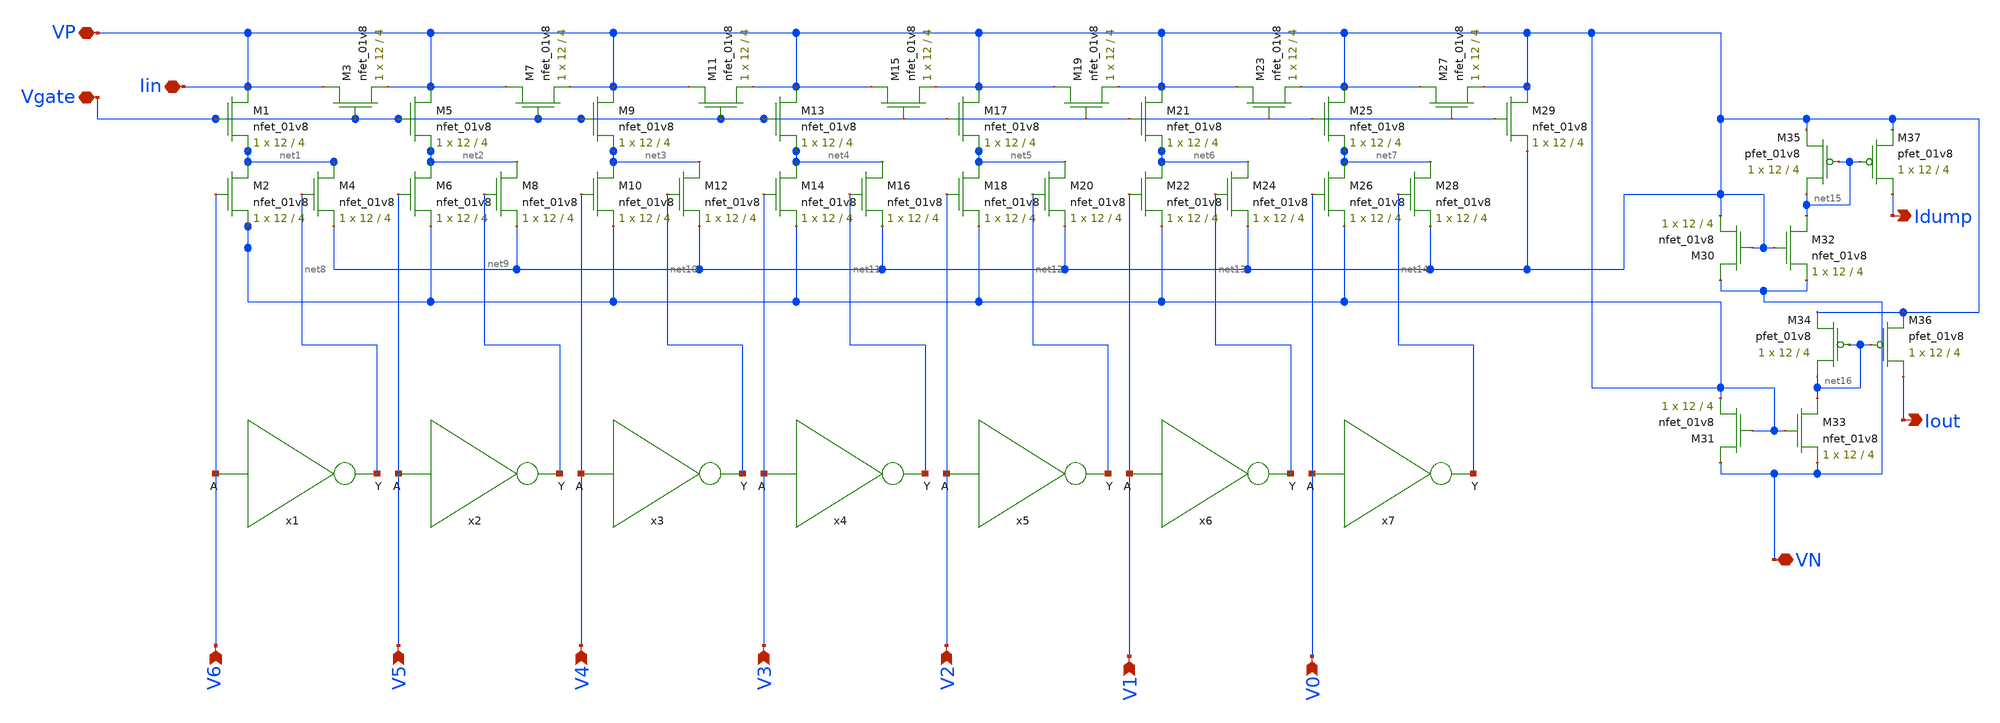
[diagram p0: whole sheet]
** sch_path: xschem/ladder_andrew.sch
**.subckt ladder_andrew V6 V5 V4 V3 V2 V1 V0 VP Iin Iout Idump VN Vgate
*.ipin V6
*.ipin V5
*.ipin V4
*.ipin V3
*.ipin V2
*.ipin V1
*.ipin V0
*.iopin VP
*.iopin Iin
*.opin Iout
*.opin Idump
*.iopin VN
*.iopin Vgate
XM1 VP Vgate net1 GND sky130_fd_pr__nfet_01v8 L=4 W=12 nf=1 ad='int((nf+1)/2) * W/nf * 0.29' as='int((nf+2)/2) * W/nf * 0.29'
+ pd='2*int((nf+1)/2) * (W/nf + 0.29)' ps='2*int((nf+2)/2) * (W/nf + 0.29)' nrd='0.29 / W' nrs='0.29 / W'
+ sa=0 sb=0 sd=0 mult=1 m=1
XM3 VP Vgate VP GND sky130_fd_pr__nfet_01v8 L=4 W=12 nf=1 ad='int((nf+1)/2) * W/nf * 0.29' as='int((nf+2)/2) * W/nf * 0.29'
+ pd='2*int((nf+1)/2) * (W/nf + 0.29)' ps='2*int((nf+2)/2) * (W/nf + 0.29)' nrd='0.29 / W' nrs='0.29 / W'
+ sa=0 sb=0 sd=0 mult=1 m=1
XM5 VP Vgate net2 GND sky130_fd_pr__nfet_01v8 L=4 W=12 nf=1 ad='int((nf+1)/2) * W/nf * 0.29' as='int((nf+2)/2) * W/nf * 0.29'
+ pd='2*int((nf+1)/2) * (W/nf + 0.29)' ps='2*int((nf+2)/2) * (W/nf + 0.29)' nrd='0.29 / W' nrs='0.29 / W'
+ sa=0 sb=0 sd=0 mult=1 m=1
XM7 VP Vgate VP GND sky130_fd_pr__nfet_01v8 L=4 W=12 nf=1 ad='int((nf+1)/2) * W/nf * 0.29' as='int((nf+2)/2) * W/nf * 0.29'
+ pd='2*int((nf+1)/2) * (W/nf + 0.29)' ps='2*int((nf+2)/2) * (W/nf + 0.29)' nrd='0.29 / W' nrs='0.29 / W'
+ sa=0 sb=0 sd=0 mult=1 m=1
XM6 net2 V5 VP GND sky130_fd_pr__nfet_01v8 L=4 W=12 nf=1 ad='int((nf+1)/2) * W/nf * 0.29' as='int((nf+2)/2) * W/nf * 0.29'
+ pd='2*int((nf+1)/2) * (W/nf + 0.29)' ps='2*int((nf+2)/2) * (W/nf + 0.29)' nrd='0.29 / W' nrs='0.29 / W'
+ sa=0 sb=0 sd=0 mult=1 m=1
XM8 net2 net9 VP GND sky130_fd_pr__nfet_01v8 L=4 W=12 nf=1 ad='int((nf+1)/2) * W/nf * 0.29' as='int((nf+2)/2) * W/nf * 0.29'
+ pd='2*int((nf+1)/2) * (W/nf + 0.29)' ps='2*int((nf+2)/2) * (W/nf + 0.29)' nrd='0.29 / W' nrs='0.29 / W'
+ sa=0 sb=0 sd=0 mult=1 m=1
XM2 net1 V6 VP GND sky130_fd_pr__nfet_01v8 L=4 W=12 nf=1 ad='int((nf+1)/2) * W/nf * 0.29' as='int((nf+2)/2) * W/nf * 0.29'
+ pd='2*int((nf+1)/2) * (W/nf + 0.29)' ps='2*int((nf+2)/2) * (W/nf + 0.29)' nrd='0.29 / W' nrs='0.29 / W'
+ sa=0 sb=0 sd=0 mult=1 m=1
XM4 net1 net8 VP GND sky130_fd_pr__nfet_01v8 L=4 W=12 nf=1 ad='int((nf+1)/2) * W/nf * 0.29' as='int((nf+2)/2) * W/nf * 0.29'
+ pd='2*int((nf+1)/2) * (W/nf + 0.29)' ps='2*int((nf+2)/2) * (W/nf + 0.29)' nrd='0.29 / W' nrs='0.29 / W'
+ sa=0 sb=0 sd=0 mult=1 m=1
XM9 VP Vgate net3 GND sky130_fd_pr__nfet_01v8 L=4 W=12 nf=1 ad='int((nf+1)/2) * W/nf * 0.29' as='int((nf+2)/2) * W/nf * 0.29'
+ pd='2*int((nf+1)/2) * (W/nf + 0.29)' ps='2*int((nf+2)/2) * (W/nf + 0.29)' nrd='0.29 / W' nrs='0.29 / W'
+ sa=0 sb=0 sd=0 mult=1 m=1
XM11 VP Vgate VP GND sky130_fd_pr__nfet_01v8 L=4 W=12 nf=1 ad='int((nf+1)/2) * W/nf * 0.29' as='int((nf+2)/2) * W/nf * 0.29'
+ pd='2*int((nf+1)/2) * (W/nf + 0.29)' ps='2*int((nf+2)/2) * (W/nf + 0.29)' nrd='0.29 / W' nrs='0.29 / W'
+ sa=0 sb=0 sd=0 mult=1 m=1
XM10 net3 V4 VP GND sky130_fd_pr__nfet_01v8 L=4 W=12 nf=1 ad='int((nf+1)/2) * W/nf * 0.29' as='int((nf+2)/2) * W/nf * 0.29'
+ pd='2*int((nf+1)/2) * (W/nf + 0.29)' ps='2*int((nf+2)/2) * (W/nf + 0.29)' nrd='0.29 / W' nrs='0.29 / W'
+ sa=0 sb=0 sd=0 mult=1 m=1
XM12 net3 net10 VP GND sky130_fd_pr__nfet_01v8 L=4 W=12 nf=1 ad='int((nf+1)/2) * W/nf * 0.29' as='int((nf+2)/2) * W/nf * 0.29'
+ pd='2*int((nf+1)/2) * (W/nf + 0.29)' ps='2*int((nf+2)/2) * (W/nf + 0.29)' nrd='0.29 / W' nrs='0.29 / W'
+ sa=0 sb=0 sd=0 mult=1 m=1
XM13 VP Vgate net4 GND sky130_fd_pr__nfet_01v8 L=4 W=12 nf=1 ad='int((nf+1)/2) * W/nf * 0.29' as='int((nf+2)/2) * W/nf * 0.29'
+ pd='2*int((nf+1)/2) * (W/nf + 0.29)' ps='2*int((nf+2)/2) * (W/nf + 0.29)' nrd='0.29 / W' nrs='0.29 / W'
+ sa=0 sb=0 sd=0 mult=1 m=1
XM15 VP Vgate VP GND sky130_fd_pr__nfet_01v8 L=4 W=12 nf=1 ad='int((nf+1)/2) * W/nf * 0.29' as='int((nf+2)/2) * W/nf * 0.29'
+ pd='2*int((nf+1)/2) * (W/nf + 0.29)' ps='2*int((nf+2)/2) * (W/nf + 0.29)' nrd='0.29 / W' nrs='0.29 / W'
+ sa=0 sb=0 sd=0 mult=1 m=1
XM14 net4 V3 VP GND sky130_fd_pr__nfet_01v8 L=4 W=12 nf=1 ad='int((nf+1)/2) * W/nf * 0.29' as='int((nf+2)/2) * W/nf * 0.29'
+ pd='2*int((nf+1)/2) * (W/nf + 0.29)' ps='2*int((nf+2)/2) * (W/nf + 0.29)' nrd='0.29 / W' nrs='0.29 / W'
+ sa=0 sb=0 sd=0 mult=1 m=1
XM16 net4 net11 VP GND sky130_fd_pr__nfet_01v8 L=4 W=12 nf=1 ad='int((nf+1)/2) * W/nf * 0.29' as='int((nf+2)/2) * W/nf * 0.29'
+ pd='2*int((nf+1)/2) * (W/nf + 0.29)' ps='2*int((nf+2)/2) * (W/nf + 0.29)' nrd='0.29 / W' nrs='0.29 / W'
+ sa=0 sb=0 sd=0 mult=1 m=1
XM17 VP Vgate net5 GND sky130_fd_pr__nfet_01v8 L=4 W=12 nf=1 ad='int((nf+1)/2) * W/nf * 0.29' as='int((nf+2)/2) * W/nf * 0.29'
+ pd='2*int((nf+1)/2) * (W/nf + 0.29)' ps='2*int((nf+2)/2) * (W/nf + 0.29)' nrd='0.29 / W' nrs='0.29 / W'
+ sa=0 sb=0 sd=0 mult=1 m=1
XM19 VP Vgate VP GND sky130_fd_pr__nfet_01v8 L=4 W=12 nf=1 ad='int((nf+1)/2) * W/nf * 0.29' as='int((nf+2)/2) * W/nf * 0.29'
+ pd='2*int((nf+1)/2) * (W/nf + 0.29)' ps='2*int((nf+2)/2) * (W/nf + 0.29)' nrd='0.29 / W' nrs='0.29 / W'
+ sa=0 sb=0 sd=0 mult=1 m=1
XM18 net5 V2 VP GND sky130_fd_pr__nfet_01v8 L=4 W=12 nf=1 ad='int((nf+1)/2) * W/nf * 0.29' as='int((nf+2)/2) * W/nf * 0.29'
+ pd='2*int((nf+1)/2) * (W/nf + 0.29)' ps='2*int((nf+2)/2) * (W/nf + 0.29)' nrd='0.29 / W' nrs='0.29 / W'
+ sa=0 sb=0 sd=0 mult=1 m=1
XM20 net5 net12 VP GND sky130_fd_pr__nfet_01v8 L=4 W=12 nf=1 ad='int((nf+1)/2) * W/nf * 0.29' as='int((nf+2)/2) * W/nf * 0.29'
+ pd='2*int((nf+1)/2) * (W/nf + 0.29)' ps='2*int((nf+2)/2) * (W/nf + 0.29)' nrd='0.29 / W' nrs='0.29 / W'
+ sa=0 sb=0 sd=0 mult=1 m=1
XM21 VP Vgate net6 GND sky130_fd_pr__nfet_01v8 L=4 W=12 nf=1 ad='int((nf+1)/2) * W/nf * 0.29' as='int((nf+2)/2) * W/nf * 0.29'
+ pd='2*int((nf+1)/2) * (W/nf + 0.29)' ps='2*int((nf+2)/2) * (W/nf + 0.29)' nrd='0.29 / W' nrs='0.29 / W'
+ sa=0 sb=0 sd=0 mult=1 m=1
XM23 VP Vgate VP GND sky130_fd_pr__nfet_01v8 L=4 W=12 nf=1 ad='int((nf+1)/2) * W/nf * 0.29' as='int((nf+2)/2) * W/nf * 0.29'
+ pd='2*int((nf+1)/2) * (W/nf + 0.29)' ps='2*int((nf+2)/2) * (W/nf + 0.29)' nrd='0.29 / W' nrs='0.29 / W'
+ sa=0 sb=0 sd=0 mult=1 m=1
XM22 net6 V1 VP GND sky130_fd_pr__nfet_01v8 L=4 W=12 nf=1 ad='int((nf+1)/2) * W/nf * 0.29' as='int((nf+2)/2) * W/nf * 0.29'
+ pd='2*int((nf+1)/2) * (W/nf + 0.29)' ps='2*int((nf+2)/2) * (W/nf + 0.29)' nrd='0.29 / W' nrs='0.29 / W'
+ sa=0 sb=0 sd=0 mult=1 m=1
XM24 net6 net13 VP GND sky130_fd_pr__nfet_01v8 L=4 W=12 nf=1 ad='int((nf+1)/2) * W/nf * 0.29' as='int((nf+2)/2) * W/nf * 0.29'
+ pd='2*int((nf+1)/2) * (W/nf + 0.29)' ps='2*int((nf+2)/2) * (W/nf + 0.29)' nrd='0.29 / W' nrs='0.29 / W'
+ sa=0 sb=0 sd=0 mult=1 m=1
XM25 VP Vgate net7 GND sky130_fd_pr__nfet_01v8 L=4 W=12 nf=1 ad='int((nf+1)/2) * W/nf * 0.29' as='int((nf+2)/2) * W/nf * 0.29'
+ pd='2*int((nf+1)/2) * (W/nf + 0.29)' ps='2*int((nf+2)/2) * (W/nf + 0.29)' nrd='0.29 / W' nrs='0.29 / W'
+ sa=0 sb=0 sd=0 mult=1 m=1
XM27 VP Vgate VP GND sky130_fd_pr__nfet_01v8 L=4 W=12 nf=1 ad='int((nf+1)/2) * W/nf * 0.29' as='int((nf+2)/2) * W/nf * 0.29'
+ pd='2*int((nf+1)/2) * (W/nf + 0.29)' ps='2*int((nf+2)/2) * (W/nf + 0.29)' nrd='0.29 / W' nrs='0.29 / W'
+ sa=0 sb=0 sd=0 mult=1 m=1
XM26 net7 V0 VP GND sky130_fd_pr__nfet_01v8 L=4 W=12 nf=1 ad='int((nf+1)/2) * W/nf * 0.29' as='int((nf+2)/2) * W/nf * 0.29'
+ pd='2*int((nf+1)/2) * (W/nf + 0.29)' ps='2*int((nf+2)/2) * (W/nf + 0.29)' nrd='0.29 / W' nrs='0.29 / W'
+ sa=0 sb=0 sd=0 mult=1 m=1
XM28 net7 net14 VP GND sky130_fd_pr__nfet_01v8 L=4 W=12 nf=1 ad='int((nf+1)/2) * W/nf * 0.29' as='int((nf+2)/2) * W/nf * 0.29'
+ pd='2*int((nf+1)/2) * (W/nf + 0.29)' ps='2*int((nf+2)/2) * (W/nf + 0.29)' nrd='0.29 / W' nrs='0.29 / W'
+ sa=0 sb=0 sd=0 mult=1 m=1
XM29 VP Vgate VP GND sky130_fd_pr__nfet_01v8 L=4 W=12 nf=1 ad='int((nf+1)/2) * W/nf * 0.29' as='int((nf+2)/2) * W/nf * 0.29'
+ pd='2*int((nf+1)/2) * (W/nf + 0.29)' ps='2*int((nf+2)/2) * (W/nf + 0.29)' nrd='0.29 / W' nrs='0.29 / W'
+ sa=0 sb=0 sd=0 mult=1 m=1
x1 net8 V6 inverter
x2 net9 V5 inverter
x3 net10 V4 inverter
x4 net11 V3 inverter
x5 net12 V2 inverter
x6 net13 V1 inverter
x7 net14 V0 inverter
XM30 VN VP VP GND sky130_fd_pr__nfet_01v8 L=4 W=12 nf=1 ad='int((nf+1)/2) * W/nf * 0.29' as='int((nf+2)/2) * W/nf * 0.29'
+ pd='2*int((nf+1)/2) * (W/nf + 0.29)' ps='2*int((nf+2)/2) * (W/nf + 0.29)' nrd='0.29 / W' nrs='0.29 / W'
+ sa=0 sb=0 sd=0 mult=1 m=1
XM31 VN VP VP GND sky130_fd_pr__nfet_01v8 L=4 W=12 nf=1 ad='int((nf+1)/2) * W/nf * 0.29' as='int((nf+2)/2) * W/nf * 0.29'
+ pd='2*int((nf+1)/2) * (W/nf + 0.29)' ps='2*int((nf+2)/2) * (W/nf + 0.29)' nrd='0.29 / W' nrs='0.29 / W'
+ sa=0 sb=0 sd=0 mult=1 m=1
XM32 net15 VP VN GND sky130_fd_pr__nfet_01v8 L=4 W=12 nf=1 ad='int((nf+1)/2) * W/nf * 0.29' as='int((nf+2)/2) * W/nf * 0.29'
+ pd='2*int((nf+1)/2) * (W/nf + 0.29)' ps='2*int((nf+2)/2) * (W/nf + 0.29)' nrd='0.29 / W' nrs='0.29 / W'
+ sa=0 sb=0 sd=0 mult=1 m=1
XM33 net16 VP VN GND sky130_fd_pr__nfet_01v8 L=4 W=12 nf=1 ad='int((nf+1)/2) * W/nf * 0.29' as='int((nf+2)/2) * W/nf * 0.29'
+ pd='2*int((nf+1)/2) * (W/nf + 0.29)' ps='2*int((nf+2)/2) * (W/nf + 0.29)' nrd='0.29 / W' nrs='0.29 / W'
+ sa=0 sb=0 sd=0 mult=1 m=1
XM35 net15 net15 VP VDD sky130_fd_pr__pfet_01v8 L=4 W=12 nf=1 ad='int((nf+1)/2) * W/nf * 0.29' as='int((nf+2)/2) * W/nf * 0.29'
+ pd='2*int((nf+1)/2) * (W/nf + 0.29)' ps='2*int((nf+2)/2) * (W/nf + 0.29)' nrd='0.29 / W' nrs='0.29 / W'
+ sa=0 sb=0 sd=0 mult=1 m=1
XM37 Idump net15 VP VDD sky130_fd_pr__pfet_01v8 L=4 W=12 nf=1 ad='int((nf+1)/2) * W/nf * 0.29' as='int((nf+2)/2) * W/nf * 0.29'
+ pd='2*int((nf+1)/2) * (W/nf + 0.29)' ps='2*int((nf+2)/2) * (W/nf + 0.29)' nrd='0.29 / W' nrs='0.29 / W'
+ sa=0 sb=0 sd=0 mult=1 m=1
XM34 net16 net16 VP VDD sky130_fd_pr__pfet_01v8 L=4 W=12 nf=1 ad='int((nf+1)/2) * W/nf * 0.29' as='int((nf+2)/2) * W/nf * 0.29'
+ pd='2*int((nf+1)/2) * (W/nf + 0.29)' ps='2*int((nf+2)/2) * (W/nf + 0.29)' nrd='0.29 / W' nrs='0.29 / W'
+ sa=0 sb=0 sd=0 mult=1 m=1
XM36 Iout net16 VP VDD sky130_fd_pr__pfet_01v8 L=4 W=12 nf=1 ad='int((nf+1)/2) * W/nf * 0.29' as='int((nf+2)/2) * W/nf * 0.29'
+ pd='2*int((nf+1)/2) * (W/nf + 0.29)' ps='2*int((nf+2)/2) * (W/nf + 0.29)' nrd='0.29 / W' nrs='0.29 / W'
+ sa=0 sb=0 sd=0 mult=1 m=1
**.ends

* expanding   symbol:  ./inverter.sym # of pins=2
** sym_path: xschem/inverter.sym
** sch_path: xschem/inverter.sch
.subckt inverter Y A
*.ipin A
*.opin Y
XM1 Y A VDD VDD sky130_fd_pr__pfet_01v8 L=0.15 W=1 nf=1 ad='int((nf+1)/2) * W/nf * 0.29' as='int((nf+2)/2) * W/nf * 0.29'
+ pd='2*int((nf+1)/2) * (W/nf + 0.29)' ps='2*int((nf+2)/2) * (W/nf + 0.29)' nrd='0.29 / W' nrs='0.29 / W'
+ sa=0 sb=0 sd=0 mult=1 m=1
XM2 Y A GND GND sky130_fd_pr__nfet_01v8 L=0.15 W=1 nf=1 ad='int((nf+1)/2) * W/nf * 0.29' as='int((nf+2)/2) * W/nf * 0.29'
+ pd='2*int((nf+1)/2) * (W/nf + 0.29)' ps='2*int((nf+2)/2) * (W/nf + 0.29)' nrd='0.29 / W' nrs='0.29 / W'
+ sa=0 sb=0 sd=0 mult=1 m=1
.ends

.GLOBAL GND
.GLOBAL VDD
.end
